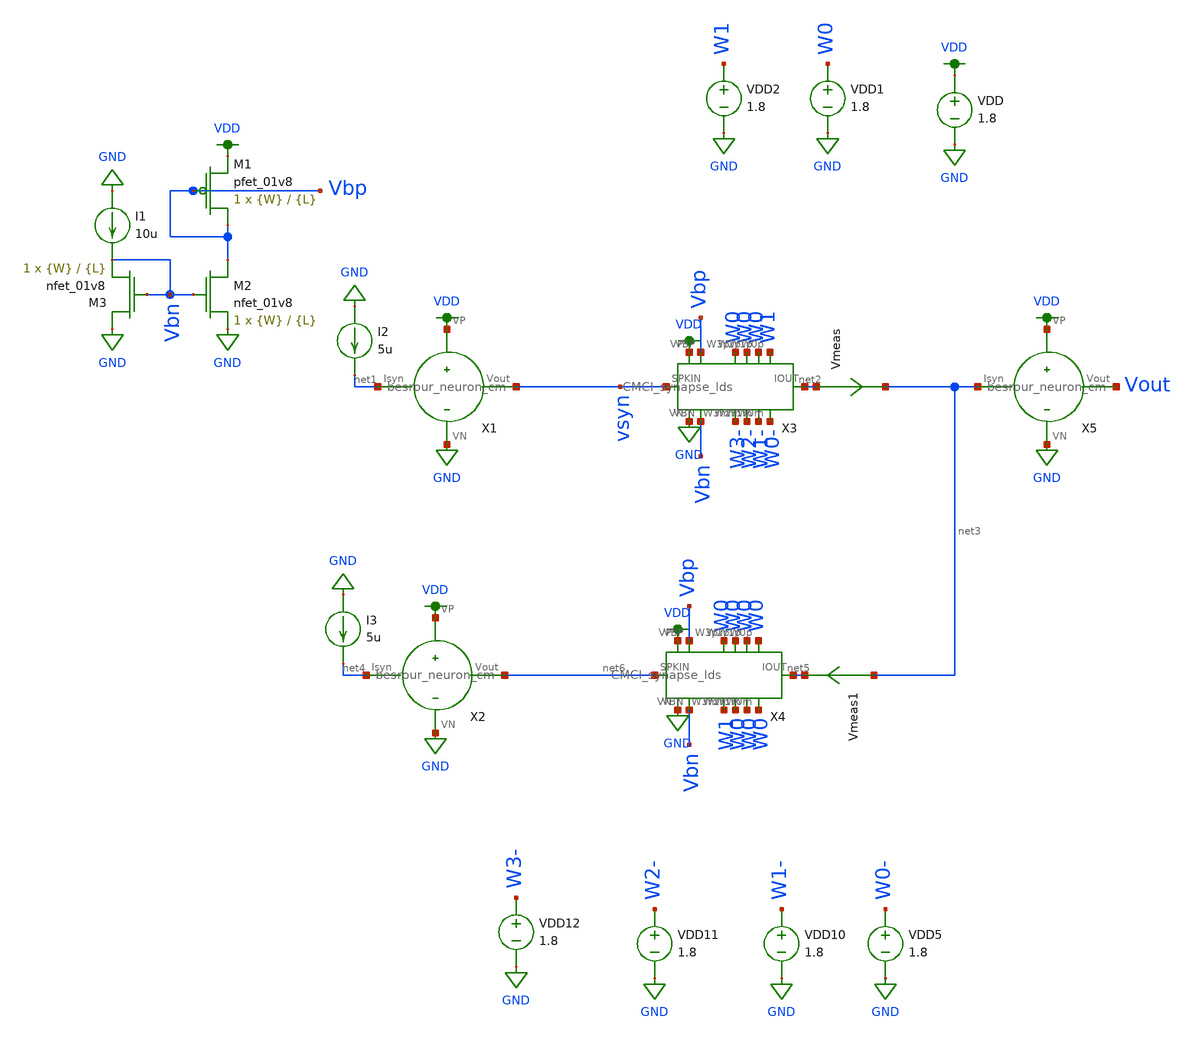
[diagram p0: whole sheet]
** sch_path: schematic/tran_CMCI.sch
**.subckt tran_CMCI
VDD VDD GND 1.8
VDD1 W0 GND 1.8
VDD2 W1 GND 1.8
Vmeas net2 net3 0
.save i(vmeas)
XM1 Vbp Vbp VDD VDD sky130_fd_pr__pfet_01v8 L={L} W={W} nf=1 ad='int((nf+1)/2) * W/nf * 0.29' as='int((nf+2)/2) * W/nf * 0.29'
+ pd='2*int((nf+1)/2) * (W/nf + 0.29)' ps='2*int((nf+2)/2) * (W/nf + 0.29)' nrd='0.29 / W' nrs='0.29 / W'
+ sa=0 sb=0 sd=0 mult=1 m=1
XM2 Vbp Vbn GND GND sky130_fd_pr__nfet_01v8 L={L} W={W} nf=1 ad='int((nf+1)/2) * W/nf * 0.29' as='int((nf+2)/2) * W/nf * 0.29'
+ pd='2*int((nf+1)/2) * (W/nf + 0.29)' ps='2*int((nf+2)/2) * (W/nf + 0.29)' nrd='0.29 / W' nrs='0.29 / W'
+ sa=0 sb=0 sd=0 mult=1 m=1
XM3 GND Vbn Vbn GND sky130_fd_pr__nfet_01v8 L={L} W={W} nf=1 ad='int((nf+1)/2) * W/nf * 0.29' as='int((nf+2)/2) * W/nf * 0.29'
+ pd='2*int((nf+1)/2) * (W/nf + 0.29)' ps='2*int((nf+2)/2) * (W/nf + 0.29)' nrd='0.29 / W' nrs='0.29 / W'
+ sa=0 sb=0 sd=0 mult=1 m=1
I1 GND Vbn 10u
I2 GND net1 5u
VDD5 W0- GND 1.8
VDD10 W1- GND 1.8
VDD11 W2- GND 1.8
VDD12 W3- GND 1.8
Vmeas1 net3 net5 0
.save i(vmeas1)
I3 GND net4 5u
X1 net1 vsyn VDD GND besrour_neuron_cm
X2 net4 net6 VDD GND besrour_neuron_cm
X5 net3 Vout VDD GND besrour_neuron_cm
X3 VDD Vbp W0 W0 W0 W1 net2 W0- W1- W2- W3- Vbn GND vsyn CMCI_synapse_lds
X4 VDD Vbp W0 W0 W0 W0 net5 W0 W0 W0 W1 Vbn GND net6 CMCI_synapse_lds
**** begin user architecture code

.param W=3
.param L=0.5
.tran 1ns 1us
.save all



.option wnflag=1
.param MC_SWITCH=0.0
.lib ~/skywater/skywater-pdk/libraries/sky130_fd_pr_ngspice/latest/models/sky130.lib.spice tt

**** end user architecture code
**.ends

* expanding   symbol:
*+  /home/madvlsi/Documents/second/neuromorphic_computing_final/schematic/besrour_neuron_cm.sym # of pins=4
** sym_path: schematic/besrour_neuron_cm.sym
** sch_path: schematic/besrour_neuron_cm.sch
.subckt besrour_neuron_cm Isyn Vout VP VN
*.iopin VP
*.iopin VN
*.iopin Isyn
*.opin Vout
XM2 VMEMINT net1 VP VDD sky130_fd_pr__pfet_01v8 L={L} W={W} nf=1 ad='int((nf+1)/2) * W/nf * 0.29' as='int((nf+2)/2) * W/nf * 0.29'
+ pd='2*int((nf+1)/2) * (W/nf + 0.29)' ps='2*int((nf+2)/2) * (W/nf + 0.29)' nrd='0.29 / W' nrs='0.29 / W'
+ sa=0 sb=0 sd=0 mult=1 m=1
XM3 VP net3 VMEMINT VDD sky130_fd_pr__pfet_01v8 L={L} W={W} nf=1 ad='int((nf+1)/2) * W/nf * 0.29' as='int((nf+2)/2) * W/nf * 0.29'
+ pd='2*int((nf+1)/2) * (W/nf + 0.29)' ps='2*int((nf+2)/2) * (W/nf + 0.29)' nrd='0.29 / W' nrs='0.29 / W'
+ sa=0 sb=0 sd=0 mult=1 m=1
XM4 net3 VMEMINT VP VDD sky130_fd_pr__pfet_01v8 L={L} W={W} nf=1 ad='int((nf+1)/2) * W/nf * 0.29' as='int((nf+2)/2) * W/nf * 0.29'
+ pd='2*int((nf+1)/2) * (W/nf + 0.29)' ps='2*int((nf+2)/2) * (W/nf + 0.29)' nrd='0.29 / W' nrs='0.29 / W'
+ sa=0 sb=0 sd=0 mult=1 m=1
XM5 net2 net3 VP VDD sky130_fd_pr__pfet_01v8 L={L} W={W} nf=1 ad='int((nf+1)/2) * W/nf * 0.29' as='int((nf+2)/2) * W/nf * 0.29'
+ pd='2*int((nf+1)/2) * (W/nf + 0.29)' ps='2*int((nf+2)/2) * (W/nf + 0.29)' nrd='0.29 / W' nrs='0.29 / W'
+ sa=0 sb=0 sd=0 mult=1 m=1
XM6 net3 VMEMINT VN GND sky130_fd_pr__nfet_01v8 L={L} W={W} nf=1 ad='int((nf+1)/2) * W/nf * 0.29' as='int((nf+2)/2) * W/nf * 0.29'
+ pd='2*int((nf+1)/2) * (W/nf + 0.29)' ps='2*int((nf+2)/2) * (W/nf + 0.29)' nrd='0.29 / W' nrs='0.29 / W'
+ sa=0 sb=0 sd=0 mult=1 m=1
XM8 net2 net3 VN GND sky130_fd_pr__nfet_01v8 L={L} W={W} nf=1 ad='int((nf+1)/2) * W/nf * 0.29' as='int((nf+2)/2) * W/nf * 0.29'
+ pd='2*int((nf+1)/2) * (W/nf + 0.29)' ps='2*int((nf+2)/2) * (W/nf + 0.29)' nrd='0.29 / W' nrs='0.29 / W'
+ sa=0 sb=0 sd=0 mult=1 m=1
C1 VMEMINT VN 340f m=1
C2 net2 VN 340f m=1
XM9 net4 net2 VP VDD sky130_fd_pr__pfet_01v8 L={L} W={W} nf=1 ad='int((nf+1)/2) * W/nf * 0.29' as='int((nf+2)/2) * W/nf * 0.29'
+ pd='2*int((nf+1)/2) * (W/nf + 0.29)' ps='2*int((nf+2)/2) * (W/nf + 0.29)' nrd='0.29 / W' nrs='0.29 / W'
+ sa=0 sb=0 sd=0 mult=1 m=1
XM10 net4 net2 VN GND sky130_fd_pr__nfet_01v8 L={L} W={W} nf=1 ad='int((nf+1)/2) * W/nf * 0.29' as='int((nf+2)/2) * W/nf * 0.29'
+ pd='2*int((nf+1)/2) * (W/nf + 0.29)' ps='2*int((nf+2)/2) * (W/nf + 0.29)' nrd='0.29 / W' nrs='0.29 / W'
+ sa=0 sb=0 sd=0 mult=1 m=1
XM11 Vout net4 VP VDD sky130_fd_pr__pfet_01v8 L={L} W={W} nf=1 ad='int((nf+1)/2) * W/nf * 0.29' as='int((nf+2)/2) * W/nf * 0.29'
+ pd='2*int((nf+1)/2) * (W/nf + 0.29)' ps='2*int((nf+2)/2) * (W/nf + 0.29)' nrd='0.29 / W' nrs='0.29 / W'
+ sa=0 sb=0 sd=0 mult=1 m=1
XM12 Vout net4 VN GND sky130_fd_pr__nfet_01v8 L={L} W={W} nf=1 ad='int((nf+1)/2) * W/nf * 0.29' as='int((nf+2)/2) * W/nf * 0.29'
+ pd='2*int((nf+1)/2) * (W/nf + 0.29)' ps='2*int((nf+2)/2) * (W/nf + 0.29)' nrd='0.29 / W' nrs='0.29 / W'
+ sa=0 sb=0 sd=0 mult=1 m=1
XM13 net1 Isyn VN GND sky130_fd_pr__nfet_01v8 L={L} W={W} nf=1 ad='int((nf+1)/2) * W/nf * 0.29' as='int((nf+2)/2) * W/nf * 0.29'
+ pd='2*int((nf+1)/2) * (W/nf + 0.29)' ps='2*int((nf+2)/2) * (W/nf + 0.29)' nrd='0.29 / W' nrs='0.29 / W'
+ sa=0 sb=0 sd=0 mult=1 m=1
XM14 VN Isyn Isyn GND sky130_fd_pr__nfet_01v8 L={L} W={W} nf=1 ad='int((nf+1)/2) * W/nf * 0.29' as='int((nf+2)/2) * W/nf * 0.29'
+ pd='2*int((nf+1)/2) * (W/nf + 0.29)' ps='2*int((nf+2)/2) * (W/nf + 0.29)' nrd='0.29 / W' nrs='0.29 / W'
+ sa=0 sb=0 sd=0 mult=1 m=1
XM1 VP net1 net1 VDD sky130_fd_pr__pfet_01v8 L={L} W={W} nf=1 ad='int((nf+1)/2) * W/nf * 0.29' as='int((nf+2)/2) * W/nf * 0.29'
+ pd='2*int((nf+1)/2) * (W/nf + 0.29)' ps='2*int((nf+2)/2) * (W/nf + 0.29)' nrd='0.29 / W' nrs='0.29 / W'
+ sa=0 sb=0 sd=0 mult=1 m=1
XM7 VN net2 VMEMINT GND sky130_fd_pr__nfet_01v8 L={L} W={W} nf=1 ad='int((nf+1)/2) * W/nf * 0.29' as='int((nf+2)/2) * W/nf * 0.29'
+ pd='2*int((nf+1)/2) * (W/nf + 0.29)' ps='2*int((nf+2)/2) * (W/nf + 0.29)' nrd='0.29 / W' nrs='0.29 / W'
+ sa=0 sb=0 sd=0 mult=1 m=1
.ends


* expanding   symbol:
*+  /home/madvlsi/Documents/second/neuromorphic_computing_final/schematic/CMCI_synapse_lds.sym # of pins=14
** sym_path: schematic/CMCI_synapse_lds.sym
** sch_path: schematic/CMCI_synapse_lds.sch
.subckt CMCI_synapse_lds VP VBP W3p W2p W1p W0p IOUT W0m W1m W2m W3m VBN VN SPKIN
*.iopin VBN
*.iopin W3p
*.iopin W2p
*.iopin W0p
*.iopin W1p
*.iopin VBP
*.iopin W3m
*.iopin W2m
*.iopin W0m
*.iopin W1m
*.opin IOUT
*.iopin SPKIN
*.iopin VP
*.iopin VN
XM36 VN net5 net5 VN sky130_fd_pr__nfet_01v8 L=0.5 W=3 nf=1 ad='int((nf+1)/2) * W/nf * 0.29' as='int((nf+2)/2) * W/nf * 0.29'
+ pd='2*int((nf+1)/2) * (W/nf + 0.29)' ps='2*int((nf+2)/2) * (W/nf + 0.29)' nrd='0.29 / W' nrs='0.29 / W'
+ sa=0 sb=0 sd=0 mult=1 m=1
XM31 net12 VBP VP VP sky130_fd_pr__pfet_01v8 L=0.5 W=3 nf=1 ad='int((nf+1)/2) * W/nf * 0.29' as='int((nf+2)/2) * W/nf * 0.29'
+ pd='2*int((nf+1)/2) * (W/nf + 0.29)' ps='2*int((nf+2)/2) * (W/nf + 0.29)' nrd='0.29 / W' nrs='0.29 / W'
+ sa=0 sb=0 sd=0 mult=1 m=1
XM18 VP VBP net12 VP sky130_fd_pr__pfet_01v8 L=0.5 W=3 nf=1 ad='int((nf+1)/2) * W/nf * 0.29' as='int((nf+2)/2) * W/nf * 0.29'
+ pd='2*int((nf+1)/2) * (W/nf + 0.29)' ps='2*int((nf+2)/2) * (W/nf + 0.29)' nrd='0.29 / W' nrs='0.29 / W'
+ sa=0 sb=0 sd=0 mult=1 m=1
XM19 net12 W1m net5 VP sky130_fd_pr__pfet_01v8 L=0.5 W=3 nf=1 ad='int((nf+1)/2) * W/nf * 0.29' as='int((nf+2)/2) * W/nf * 0.29'
+ pd='2*int((nf+1)/2) * (W/nf + 0.29)' ps='2*int((nf+2)/2) * (W/nf + 0.29)' nrd='0.29 / W' nrs='0.29 / W'
+ sa=0 sb=0 sd=0 mult=1 m=1
XM20 net5 W0m net13 VP sky130_fd_pr__pfet_01v8 L=0.5 W=3 nf=1 ad='int((nf+1)/2) * W/nf * 0.29' as='int((nf+2)/2) * W/nf * 0.29'
+ pd='2*int((nf+1)/2) * (W/nf + 0.29)' ps='2*int((nf+2)/2) * (W/nf + 0.29)' nrd='0.29 / W' nrs='0.29 / W'
+ sa=0 sb=0 sd=0 mult=1 m=1
XM21 net13 VBP VP VP sky130_fd_pr__pfet_01v8 L=0.5 W=3 nf=1 ad='int((nf+1)/2) * W/nf * 0.29' as='int((nf+2)/2) * W/nf * 0.29'
+ pd='2*int((nf+1)/2) * (W/nf + 0.29)' ps='2*int((nf+2)/2) * (W/nf + 0.29)' nrd='0.29 / W' nrs='0.29 / W'
+ sa=0 sb=0 sd=0 mult=1 m=1
XM22 VP VBP net11 VP sky130_fd_pr__pfet_01v8 L=0.5 W=3 nf=1 ad='int((nf+1)/2) * W/nf * 0.29' as='int((nf+2)/2) * W/nf * 0.29'
+ pd='2*int((nf+1)/2) * (W/nf + 0.29)' ps='2*int((nf+2)/2) * (W/nf + 0.29)' nrd='0.29 / W' nrs='0.29 / W'
+ sa=0 sb=0 sd=0 mult=1 m=1
XM23 net11 W2m net4 VP sky130_fd_pr__pfet_01v8 L=0.5 W=3 nf=1 ad='int((nf+1)/2) * W/nf * 0.29' as='int((nf+2)/2) * W/nf * 0.29'
+ pd='2*int((nf+1)/2) * (W/nf + 0.29)' ps='2*int((nf+2)/2) * (W/nf + 0.29)' nrd='0.29 / W' nrs='0.29 / W'
+ sa=0 sb=0 sd=0 mult=1 m=1
XM24 net4 W3m net10 VP sky130_fd_pr__pfet_01v8 L=0.5 W=3 nf=1 ad='int((nf+1)/2) * W/nf * 0.29' as='int((nf+2)/2) * W/nf * 0.29'
+ pd='2*int((nf+1)/2) * (W/nf + 0.29)' ps='2*int((nf+2)/2) * (W/nf + 0.29)' nrd='0.29 / W' nrs='0.29 / W'
+ sa=0 sb=0 sd=0 mult=1 m=1
XM25 net10 VBP VP VP sky130_fd_pr__pfet_01v8 L=0.5 W=3 nf=1 ad='int((nf+1)/2) * W/nf * 0.29' as='int((nf+2)/2) * W/nf * 0.29'
+ pd='2*int((nf+1)/2) * (W/nf + 0.29)' ps='2*int((nf+2)/2) * (W/nf + 0.29)' nrd='0.29 / W' nrs='0.29 / W'
+ sa=0 sb=0 sd=0 mult=1 m=1
XM26 VP VBP net10 VP sky130_fd_pr__pfet_01v8 L=0.5 W=3 nf=1 ad='int((nf+1)/2) * W/nf * 0.29' as='int((nf+2)/2) * W/nf * 0.29'
+ pd='2*int((nf+1)/2) * (W/nf + 0.29)' ps='2*int((nf+2)/2) * (W/nf + 0.29)' nrd='0.29 / W' nrs='0.29 / W'
+ sa=0 sb=0 sd=0 mult=1 m=1
XM27 net14 SPKIN VP VP sky130_fd_pr__pfet_01v8 L=0.5 W=3 nf=1 ad='int((nf+1)/2) * W/nf * 0.29' as='int((nf+2)/2) * W/nf * 0.29'
+ pd='2*int((nf+1)/2) * (W/nf + 0.29)' ps='2*int((nf+2)/2) * (W/nf + 0.29)' nrd='0.29 / W' nrs='0.29 / W'
+ sa=0 sb=0 sd=0 mult=1 m=1
XM28 IOUT net14 net9 VP sky130_fd_pr__pfet_01v8 L=0.5 W=3 nf=1 ad='int((nf+1)/2) * W/nf * 0.29' as='int((nf+2)/2) * W/nf * 0.29'
+ pd='2*int((nf+1)/2) * (W/nf + 0.29)' ps='2*int((nf+2)/2) * (W/nf + 0.29)' nrd='0.29 / W' nrs='0.29 / W'
+ sa=0 sb=0 sd=0 mult=1 m=1
XM29 net8 net8 VP VP sky130_fd_pr__pfet_01v8 L=0.5 W=3 nf=1 ad='int((nf+1)/2) * W/nf * 0.29' as='int((nf+2)/2) * W/nf * 0.29'
+ pd='2*int((nf+1)/2) * (W/nf + 0.29)' ps='2*int((nf+2)/2) * (W/nf + 0.29)' nrd='0.29 / W' nrs='0.29 / W'
+ sa=0 sb=0 sd=0 mult=1 m=1
XM30 VP net8 net9 VP sky130_fd_pr__pfet_01v8 L=0.5 W=3 nf=1 ad='int((nf+1)/2) * W/nf * 0.29' as='int((nf+2)/2) * W/nf * 0.29'
+ pd='2*int((nf+1)/2) * (W/nf + 0.29)' ps='2*int((nf+2)/2) * (W/nf + 0.29)' nrd='0.29 / W' nrs='0.29 / W'
+ sa=0 sb=0 sd=0 mult=1 m=1
XM32 VP net1 net9 VP sky130_fd_pr__pfet_01v8 L=0.5 W=3 nf=1 ad='int((nf+1)/2) * W/nf * 0.29' as='int((nf+2)/2) * W/nf * 0.29'
+ pd='2*int((nf+1)/2) * (W/nf + 0.29)' ps='2*int((nf+2)/2) * (W/nf + 0.29)' nrd='0.29 / W' nrs='0.29 / W'
+ sa=0 sb=0 sd=0 mult=1 m=1
XM33 net9 net1 VP VP sky130_fd_pr__pfet_01v8 L=0.5 W=3 nf=1 ad='int((nf+1)/2) * W/nf * 0.29' as='int((nf+2)/2) * W/nf * 0.29'
+ pd='2*int((nf+1)/2) * (W/nf + 0.29)' ps='2*int((nf+2)/2) * (W/nf + 0.29)' nrd='0.29 / W' nrs='0.29 / W'
+ sa=0 sb=0 sd=0 mult=1 m=1
XM34 VP net1 net9 VP sky130_fd_pr__pfet_01v8 L=0.5 W=3 nf=1 ad='int((nf+1)/2) * W/nf * 0.29' as='int((nf+2)/2) * W/nf * 0.29'
+ pd='2*int((nf+1)/2) * (W/nf + 0.29)' ps='2*int((nf+2)/2) * (W/nf + 0.29)' nrd='0.29 / W' nrs='0.29 / W'
+ sa=0 sb=0 sd=0 mult=1 m=1
XM37 net9 net1 VP VP sky130_fd_pr__pfet_01v8 L=0.5 W=3 nf=1 ad='int((nf+1)/2) * W/nf * 0.29' as='int((nf+2)/2) * W/nf * 0.29'
+ pd='2*int((nf+1)/2) * (W/nf + 0.29)' ps='2*int((nf+2)/2) * (W/nf + 0.29)' nrd='0.29 / W' nrs='0.29 / W'
+ sa=0 sb=0 sd=0 mult=1 m=1
XM38 VP net1 net1 VP sky130_fd_pr__pfet_01v8 L=0.5 W=3 nf=1 ad='int((nf+1)/2) * W/nf * 0.29' as='int((nf+2)/2) * W/nf * 0.29'
+ pd='2*int((nf+1)/2) * (W/nf + 0.29)' ps='2*int((nf+2)/2) * (W/nf + 0.29)' nrd='0.29 / W' nrs='0.29 / W'
+ sa=0 sb=0 sd=0 mult=1 m=1
XM1 net9 net5 VN VN sky130_fd_pr__nfet_01v8 L=0.5 W=3 nf=1 ad='int((nf+1)/2) * W/nf * 0.29' as='int((nf+2)/2) * W/nf * 0.29'
+ pd='2*int((nf+1)/2) * (W/nf + 0.29)' ps='2*int((nf+2)/2) * (W/nf + 0.29)' nrd='0.29 / W' nrs='0.29 / W'
+ sa=0 sb=0 sd=0 mult=1 m=1
XM2 net9 net4 VN VN sky130_fd_pr__nfet_01v8 L=0.5 W=3 nf=1 ad='int((nf+1)/2) * W/nf * 0.29' as='int((nf+2)/2) * W/nf * 0.29'
+ pd='2*int((nf+1)/2) * (W/nf + 0.29)' ps='2*int((nf+2)/2) * (W/nf + 0.29)' nrd='0.29 / W' nrs='0.29 / W'
+ sa=0 sb=0 sd=0 mult=1 m=1
XM3 VN net4 net9 VN sky130_fd_pr__nfet_01v8 L=0.5 W=3 nf=1 ad='int((nf+1)/2) * W/nf * 0.29' as='int((nf+2)/2) * W/nf * 0.29'
+ pd='2*int((nf+1)/2) * (W/nf + 0.29)' ps='2*int((nf+2)/2) * (W/nf + 0.29)' nrd='0.29 / W' nrs='0.29 / W'
+ sa=0 sb=0 sd=0 mult=1 m=1
XM4 net9 net4 VN VN sky130_fd_pr__nfet_01v8 L=0.5 W=3 nf=1 ad='int((nf+1)/2) * W/nf * 0.29' as='int((nf+2)/2) * W/nf * 0.29'
+ pd='2*int((nf+1)/2) * (W/nf + 0.29)' ps='2*int((nf+2)/2) * (W/nf + 0.29)' nrd='0.29 / W' nrs='0.29 / W'
+ sa=0 sb=0 sd=0 mult=1 m=1
XM5 VN net4 net9 VN sky130_fd_pr__nfet_01v8 L=0.5 W=3 nf=1 ad='int((nf+1)/2) * W/nf * 0.29' as='int((nf+2)/2) * W/nf * 0.29'
+ pd='2*int((nf+1)/2) * (W/nf + 0.29)' ps='2*int((nf+2)/2) * (W/nf + 0.29)' nrd='0.29 / W' nrs='0.29 / W'
+ sa=0 sb=0 sd=0 mult=1 m=1
XM6 net4 net4 VN VN sky130_fd_pr__nfet_01v8 L=0.5 W=3 nf=1 ad='int((nf+1)/2) * W/nf * 0.29' as='int((nf+2)/2) * W/nf * 0.29'
+ pd='2*int((nf+1)/2) * (W/nf + 0.29)' ps='2*int((nf+2)/2) * (W/nf + 0.29)' nrd='0.29 / W' nrs='0.29 / W'
+ sa=0 sb=0 sd=0 mult=1 m=1
XM7 net9 SPKIN IOUT VN sky130_fd_pr__nfet_01v8 L=0.5 W=3 nf=1 ad='int((nf+1)/2) * W/nf * 0.29' as='int((nf+2)/2) * W/nf * 0.29'
+ pd='2*int((nf+1)/2) * (W/nf + 0.29)' ps='2*int((nf+2)/2) * (W/nf + 0.29)' nrd='0.29 / W' nrs='0.29 / W'
+ sa=0 sb=0 sd=0 mult=1 m=1
XM8 net14 SPKIN VN VN sky130_fd_pr__nfet_01v8 L=0.5 W=3 nf=1 ad='int((nf+1)/2) * W/nf * 0.29' as='int((nf+2)/2) * W/nf * 0.29'
+ pd='2*int((nf+1)/2) * (W/nf + 0.29)' ps='2*int((nf+2)/2) * (W/nf + 0.29)' nrd='0.29 / W' nrs='0.29 / W'
+ sa=0 sb=0 sd=0 mult=1 m=1
XM9 VN VBN net6 VN sky130_fd_pr__nfet_01v8 L=0.5 W=3 nf=1 ad='int((nf+1)/2) * W/nf * 0.29' as='int((nf+2)/2) * W/nf * 0.29'
+ pd='2*int((nf+1)/2) * (W/nf + 0.29)' ps='2*int((nf+2)/2) * (W/nf + 0.29)' nrd='0.29 / W' nrs='0.29 / W'
+ sa=0 sb=0 sd=0 mult=1 m=1
XM10 net6 VBN VN VN sky130_fd_pr__nfet_01v8 L=0.5 W=3 nf=1 ad='int((nf+1)/2) * W/nf * 0.29' as='int((nf+2)/2) * W/nf * 0.29'
+ pd='2*int((nf+1)/2) * (W/nf + 0.29)' ps='2*int((nf+2)/2) * (W/nf + 0.29)' nrd='0.29 / W' nrs='0.29 / W'
+ sa=0 sb=0 sd=0 mult=1 m=1
XM11 net8 W1p net6 VN sky130_fd_pr__nfet_01v8 L=0.5 W=3 nf=1 ad='int((nf+1)/2) * W/nf * 0.29' as='int((nf+2)/2) * W/nf * 0.29'
+ pd='2*int((nf+1)/2) * (W/nf + 0.29)' ps='2*int((nf+2)/2) * (W/nf + 0.29)' nrd='0.29 / W' nrs='0.29 / W'
+ sa=0 sb=0 sd=0 mult=1 m=1
XM12 net7 W0p net8 VN sky130_fd_pr__nfet_01v8 L=0.5 W=3 nf=1 ad='int((nf+1)/2) * W/nf * 0.29' as='int((nf+2)/2) * W/nf * 0.29'
+ pd='2*int((nf+1)/2) * (W/nf + 0.29)' ps='2*int((nf+2)/2) * (W/nf + 0.29)' nrd='0.29 / W' nrs='0.29 / W'
+ sa=0 sb=0 sd=0 mult=1 m=1
XM13 VN VBN net7 VN sky130_fd_pr__nfet_01v8 L=0.5 W=3 nf=1 ad='int((nf+1)/2) * W/nf * 0.29' as='int((nf+2)/2) * W/nf * 0.29'
+ pd='2*int((nf+1)/2) * (W/nf + 0.29)' ps='2*int((nf+2)/2) * (W/nf + 0.29)' nrd='0.29 / W' nrs='0.29 / W'
+ sa=0 sb=0 sd=0 mult=1 m=1
XM14 net3 VBN VN VN sky130_fd_pr__nfet_01v8 L=0.5 W=3 nf=1 ad='int((nf+1)/2) * W/nf * 0.29' as='int((nf+2)/2) * W/nf * 0.29'
+ pd='2*int((nf+1)/2) * (W/nf + 0.29)' ps='2*int((nf+2)/2) * (W/nf + 0.29)' nrd='0.29 / W' nrs='0.29 / W'
+ sa=0 sb=0 sd=0 mult=1 m=1
XM15 net1 W2p net3 VN sky130_fd_pr__nfet_01v8 L=0.5 W=3 nf=1 ad='int((nf+1)/2) * W/nf * 0.29' as='int((nf+2)/2) * W/nf * 0.29'
+ pd='2*int((nf+1)/2) * (W/nf + 0.29)' ps='2*int((nf+2)/2) * (W/nf + 0.29)' nrd='0.29 / W' nrs='0.29 / W'
+ sa=0 sb=0 sd=0 mult=1 m=1
XM16 net2 W3p net1 VN sky130_fd_pr__nfet_01v8 L=0.5 W=3 nf=1 ad='int((nf+1)/2) * W/nf * 0.29' as='int((nf+2)/2) * W/nf * 0.29'
+ pd='2*int((nf+1)/2) * (W/nf + 0.29)' ps='2*int((nf+2)/2) * (W/nf + 0.29)' nrd='0.29 / W' nrs='0.29 / W'
+ sa=0 sb=0 sd=0 mult=1 m=1
XM17 VN VBN net2 VN sky130_fd_pr__nfet_01v8 L=0.5 W=3 nf=1 ad='int((nf+1)/2) * W/nf * 0.29' as='int((nf+2)/2) * W/nf * 0.29'
+ pd='2*int((nf+1)/2) * (W/nf + 0.29)' ps='2*int((nf+2)/2) * (W/nf + 0.29)' nrd='0.29 / W' nrs='0.29 / W'
+ sa=0 sb=0 sd=0 mult=1 m=1
XM35 net2 VBN VN VN sky130_fd_pr__nfet_01v8 L=0.5 W=3 nf=1 ad='int((nf+1)/2) * W/nf * 0.29' as='int((nf+2)/2) * W/nf * 0.29'
+ pd='2*int((nf+1)/2) * (W/nf + 0.29)' ps='2*int((nf+2)/2) * (W/nf + 0.29)' nrd='0.29 / W' nrs='0.29 / W'
+ sa=0 sb=0 sd=0 mult=1 m=1
.ends

.GLOBAL VDD
.GLOBAL GND
.end
